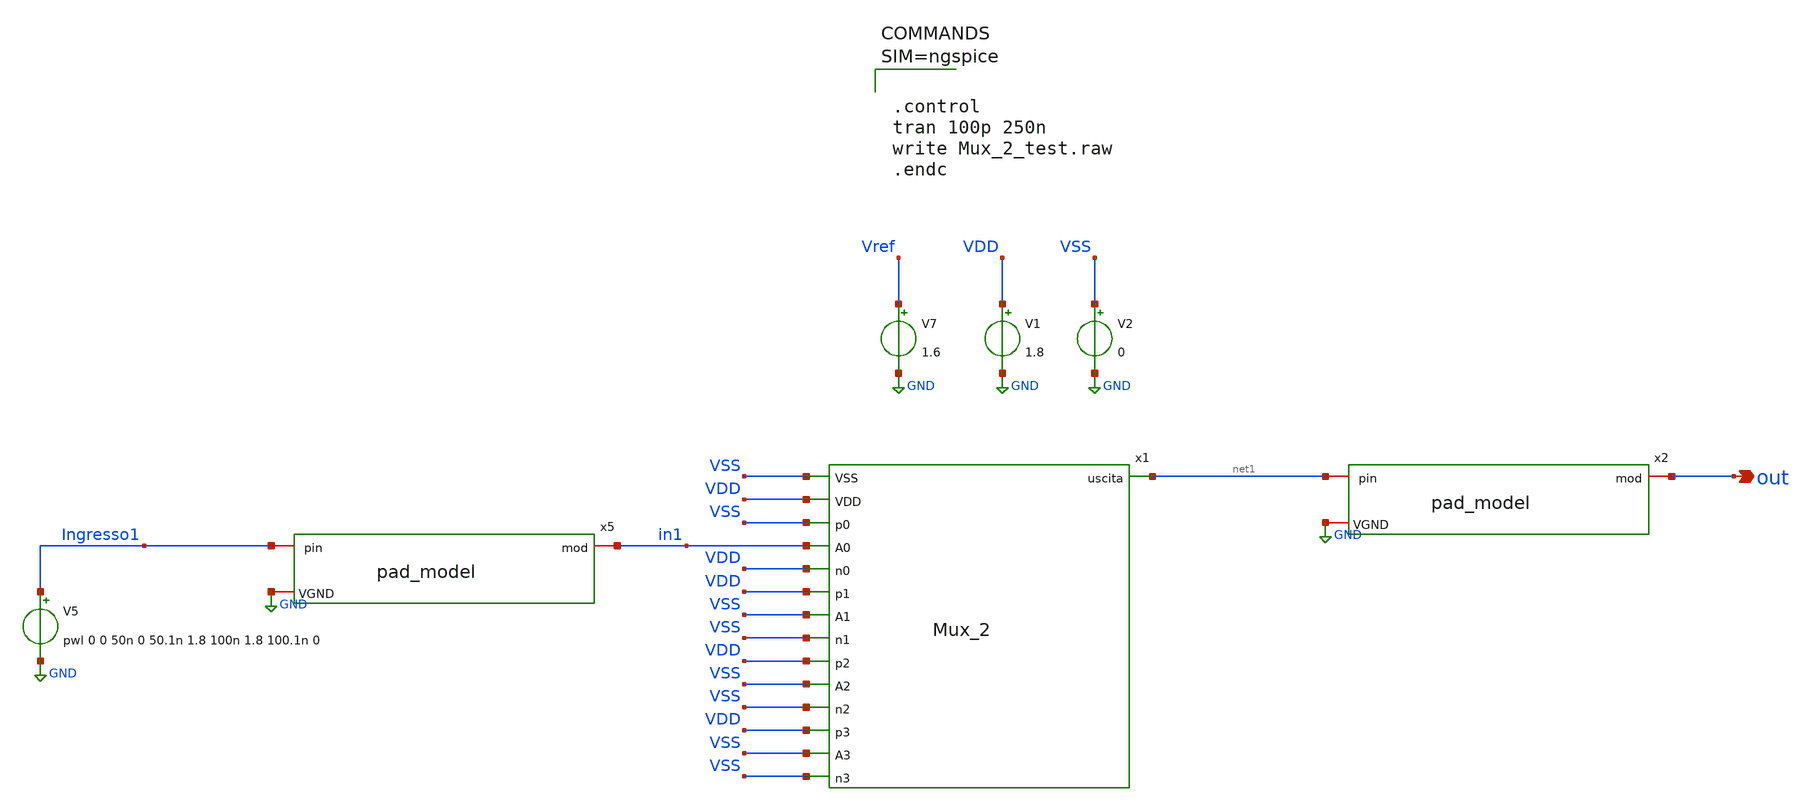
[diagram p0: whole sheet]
** sch_path: xschem/Utili/Mux_2_test.sch
**.subckt Mux_2_test out
*.opin out
V1 VDD GND 1.8
V2 VSS GND 0
V7 Vref GND 1.6
V5 Ingresso1 GND pwl 0 0 50n 0 50.1n 1.8 100n 1.8 100.1n 0
x5 GND Ingresso1 in1 pad_model
x2 GND net1 out pad_model
x1 VSS VDD VSS in1 net1 VDD VDD VSS VSS VDD VSS VSS VDD VSS VSS Mux_2
**** begin user architecture code

** opencircuitdesign pdks install
.lib $::SKYWATER_MODELS/sky130.lib.spice tt





.control
tran 100p 250n
write Mux_2_test.raw
.endc



**** end user architecture code
**.ends
.GLOBAL GND
.end
